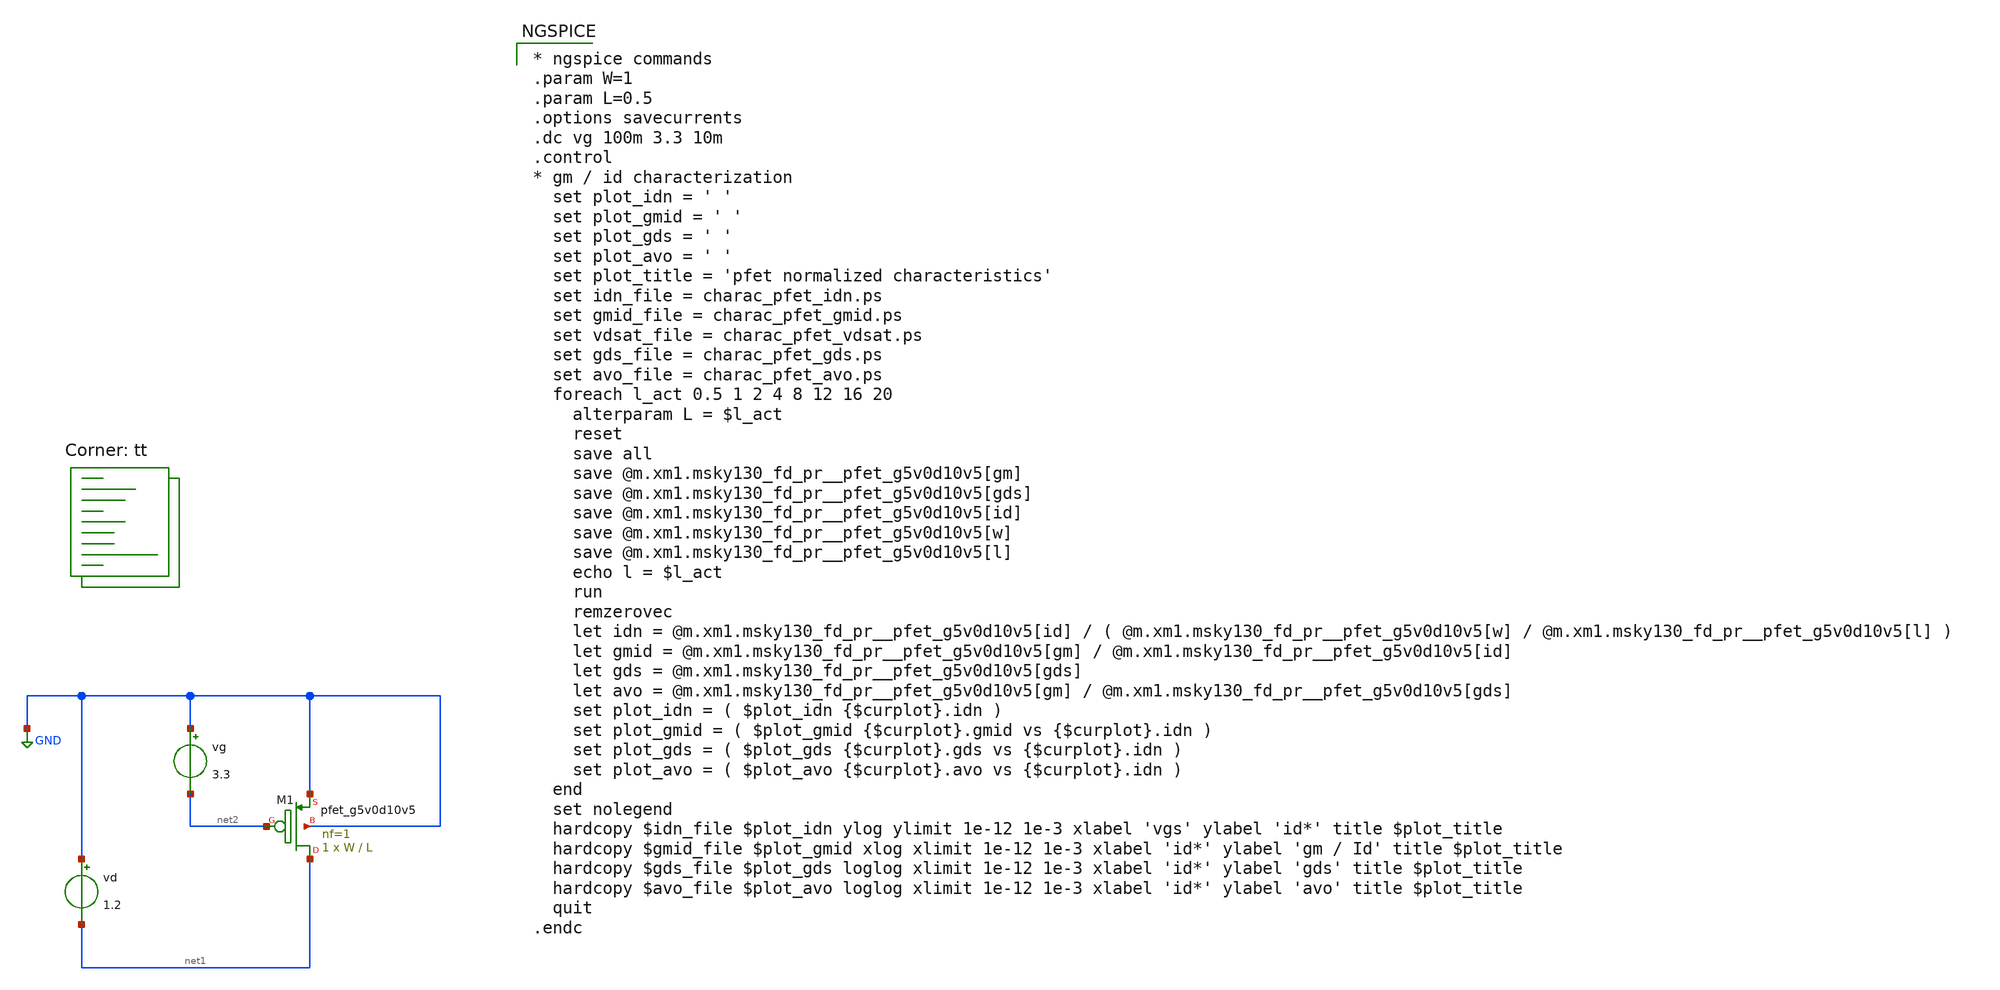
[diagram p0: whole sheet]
** sch_path: charac/gmid_pfet_tb.sch
**.subckt gmid_pfet_tb
vd GND net1 1.2
vg GND net2 3.3
XM1 net1 net2 GND GND sky130_fd_pr__pfet_g5v0d10v5 L=L W=W nf=1 ad='int((nf+1)/2) * W/nf * 0.29' as='int((nf+2)/2) * W/nf * 0.29'
+ pd='2*int((nf+1)/2) * (W/nf + 0.29)' ps='2*int((nf+2)/2) * (W/nf + 0.29)' nrd='0.29 / W' nrs='0.29 / W'
+ sa=0 sb=0 sd=0 mult=1 m=1
**** begin user architecture code
.lib $::SKYWATER_MODELS/sky130.lib.spice tt

* ngspice commands
.param W=1
.param L=0.5
.options savecurrents
.dc vg 100m 3.3 10m
.control
* gm / id characterization
  set plot_idn = ' '
  set plot_gmid = ' '
  set plot_gds = ' '
  set plot_avo = ' '
  set plot_title = 'pfet normalized characteristics'
  set idn_file = charac_pfet_idn.ps
  set gmid_file = charac_pfet_gmid.ps
  set vdsat_file = charac_pfet_vdsat.ps
  set gds_file = charac_pfet_gds.ps
  set avo_file = charac_pfet_avo.ps
  foreach l_act 0.5 1 2 4 8 12 16 20
    alterparam L = $l_act
    reset
    save all
    save @m.xm1.msky130_fd_pr__pfet_g5v0d10v5[gm]
    save @m.xm1.msky130_fd_pr__pfet_g5v0d10v5[gds]
    save @m.xm1.msky130_fd_pr__pfet_g5v0d10v5[id]
    save @m.xm1.msky130_fd_pr__pfet_g5v0d10v5[w]
    save @m.xm1.msky130_fd_pr__pfet_g5v0d10v5[l]
    echo l = $l_act
    run
    remzerovec
    let idn = @m.xm1.msky130_fd_pr__pfet_g5v0d10v5[id] / ( @m.xm1.msky130_fd_pr__pfet_g5v0d10v5[w] /
+ @m.xm1.msky130_fd_pr__pfet_g5v0d10v5[l] )
    let gmid = @m.xm1.msky130_fd_pr__pfet_g5v0d10v5[gm] / @m.xm1.msky130_fd_pr__pfet_g5v0d10v5[id]
    let gds = @m.xm1.msky130_fd_pr__pfet_g5v0d10v5[gds]
    let avo = @m.xm1.msky130_fd_pr__pfet_g5v0d10v5[gm] / @m.xm1.msky130_fd_pr__pfet_g5v0d10v5[gds]
    set plot_idn = ( $plot_idn {$curplot}.idn )
    set plot_gmid = ( $plot_gmid {$curplot}.gmid vs {$curplot}.idn )
    set plot_gds = ( $plot_gds {$curplot}.gds vs {$curplot}.idn )
    set plot_avo = ( $plot_avo {$curplot}.avo vs {$curplot}.idn )
  end
  set nolegend
  hardcopy $idn_file $plot_idn ylog ylimit 1e-12 1e-3 xlabel 'vgs' ylabel 'id*' title $plot_title
  hardcopy $gmid_file $plot_gmid xlog xlimit 1e-12 1e-3 xlabel 'id*' ylabel 'gm / Id' title $plot_title
  hardcopy $gds_file $plot_gds loglog xlimit 1e-12 1e-3 xlabel 'id*' ylabel 'gds' title $plot_title
  hardcopy $avo_file $plot_avo loglog xlimit 1e-12 1e-3 xlabel 'id*' ylabel 'avo' title $plot_title
  quit
.endc


**** end user architecture code
**.ends
.GLOBAL GND
.end
